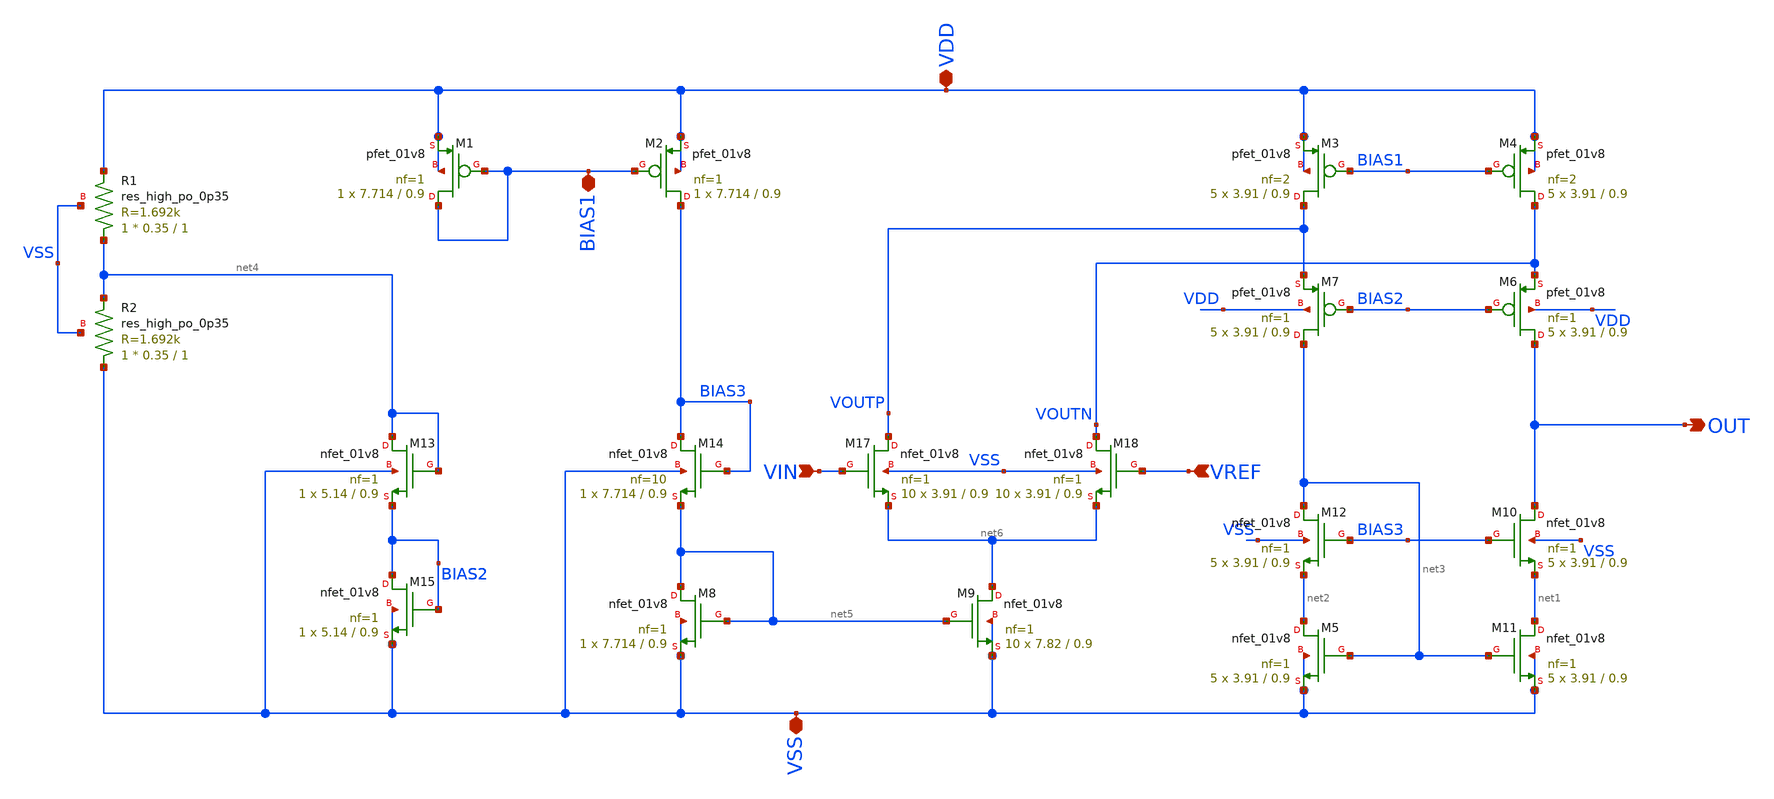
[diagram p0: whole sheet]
** sch_path: xschem/DC_DC_Converter_xschem/OTHERS/DC_DC_Converter_4/Folded_OPAMP/Folded_OPAMP_v2.sch
**.subckt Folded_OPAMP_v2 VSS VDD OUT VIN VREF BIAS1
*.iopin VSS
*.iopin VDD
*.opin OUT
*.ipin VIN
*.ipin VREF
*.iopin BIAS1
XM3 VOUTP BIAS1 VDD VDD sky130_fd_pr__pfet_01v8 L=0.9 W=3.91 nf=2 ad='int((nf+1)/2) * W/nf * 0.29' as='int((nf+2)/2) * W/nf * 0.29'
+ pd='2*int((nf+1)/2) * (W/nf + 0.29)' ps='2*int((nf+2)/2) * (W/nf + 0.29)' nrd='0.29 / W' nrs='0.29 / W'
+ sa=0 sb=0 sd=0 mult=5 m=5
XM4 VOUTN BIAS1 VDD VDD sky130_fd_pr__pfet_01v8 L=0.9 W=3.91 nf=2 ad='int((nf+1)/2) * W/nf * 0.29' as='int((nf+2)/2) * W/nf * 0.29'
+ pd='2*int((nf+1)/2) * (W/nf + 0.29)' ps='2*int((nf+2)/2) * (W/nf + 0.29)' nrd='0.29 / W' nrs='0.29 / W'
+ sa=0 sb=0 sd=0 mult=5 m=5
XM6 OUT BIAS2 VOUTN VDD sky130_fd_pr__pfet_01v8 L=0.9 W=3.91 nf=1 ad='int((nf+1)/2) * W/nf * 0.29' as='int((nf+2)/2) * W/nf * 0.29'
+ pd='2*int((nf+1)/2) * (W/nf + 0.29)' ps='2*int((nf+2)/2) * (W/nf + 0.29)' nrd='0.29 / W' nrs='0.29 / W'
+ sa=0 sb=0 sd=0 mult=5 m=5
XM7 net3 BIAS2 VOUTP VDD sky130_fd_pr__pfet_01v8 L=0.9 W=3.91 nf=1 ad='int((nf+1)/2) * W/nf * 0.29' as='int((nf+2)/2) * W/nf * 0.29'
+ pd='2*int((nf+1)/2) * (W/nf + 0.29)' ps='2*int((nf+2)/2) * (W/nf + 0.29)' nrd='0.29 / W' nrs='0.29 / W'
+ sa=0 sb=0 sd=0 mult=5 m=5
XM13 net4 net4 BIAS2 VSS sky130_fd_pr__nfet_01v8 L=0.9 W=5.14 nf=1 ad='int((nf+1)/2) * W/nf * 0.29' as='int((nf+2)/2) * W/nf * 0.29'
+ pd='2*int((nf+1)/2) * (W/nf + 0.29)' ps='2*int((nf+2)/2) * (W/nf + 0.29)' nrd='0.29 / W' nrs='0.29 / W'
+ sa=0 sb=0 sd=0 mult=1 m=1
XM14 BIAS3 BIAS3 net5 VSS sky130_fd_pr__nfet_01v8 L=0.9 W=7.714 nf=10 ad='int((nf+1)/2) * W/nf * 0.29'
+ as='int((nf+2)/2) * W/nf * 0.29' pd='2*int((nf+1)/2) * (W/nf + 0.29)' ps='2*int((nf+2)/2) * (W/nf + 0.29)'
+ nrd='0.29 / W' nrs='0.29 / W' sa=0 sb=0 sd=0 mult=1 m=1
XM15 BIAS2 BIAS2 VSS VSS sky130_fd_pr__nfet_01v8 L=0.9 W=5.14 nf=1 ad='int((nf+1)/2) * W/nf * 0.29' as='int((nf+2)/2) * W/nf * 0.29'
+ pd='2*int((nf+1)/2) * (W/nf + 0.29)' ps='2*int((nf+2)/2) * (W/nf + 0.29)' nrd='0.29 / W' nrs='0.29 / W'
+ sa=0 sb=0 sd=0 mult=1 m=1
XM17 VOUTP VIN net6 VSS sky130_fd_pr__nfet_01v8 L=0.9 W=3.91 nf=1 ad='int((nf+1)/2) * W/nf * 0.29' as='int((nf+2)/2) * W/nf * 0.29'
+ pd='2*int((nf+1)/2) * (W/nf + 0.29)' ps='2*int((nf+2)/2) * (W/nf + 0.29)' nrd='0.29 / W' nrs='0.29 / W'
+ sa=0 sb=0 sd=0 mult=10 m=10
XM18 VOUTN VREF net6 VSS sky130_fd_pr__nfet_01v8 L=0.9 W=3.91 nf=1 ad='int((nf+1)/2) * W/nf * 0.29' as='int((nf+2)/2) * W/nf * 0.29'
+ pd='2*int((nf+1)/2) * (W/nf + 0.29)' ps='2*int((nf+2)/2) * (W/nf + 0.29)' nrd='0.29 / W' nrs='0.29 / W'
+ sa=0 sb=0 sd=0 mult=10 m=10
XM10 OUT BIAS3 net1 VSS sky130_fd_pr__nfet_01v8 L=0.9 W=3.91 nf=1 ad='int((nf+1)/2) * W/nf * 0.29' as='int((nf+2)/2) * W/nf * 0.29'
+ pd='2*int((nf+1)/2) * (W/nf + 0.29)' ps='2*int((nf+2)/2) * (W/nf + 0.29)' nrd='0.29 / W' nrs='0.29 / W'
+ sa=0 sb=0 sd=0 mult=5 m=5
XM12 net3 BIAS3 net2 VSS sky130_fd_pr__nfet_01v8 L=0.9 W=3.91 nf=1 ad='int((nf+1)/2) * W/nf * 0.29' as='int((nf+2)/2) * W/nf * 0.29'
+ pd='2*int((nf+1)/2) * (W/nf + 0.29)' ps='2*int((nf+2)/2) * (W/nf + 0.29)' nrd='0.29 / W' nrs='0.29 / W'
+ sa=0 sb=0 sd=0 mult=5 m=5
XM8 net5 net5 VSS VSS sky130_fd_pr__nfet_01v8 L=0.9 W=7.714 nf=1 ad='int((nf+1)/2) * W/nf * 0.29' as='int((nf+2)/2) * W/nf * 0.29'
+ pd='2*int((nf+1)/2) * (W/nf + 0.29)' ps='2*int((nf+2)/2) * (W/nf + 0.29)' nrd='0.29 / W' nrs='0.29 / W'
+ sa=0 sb=0 sd=0 mult=1 m=1
XM9 net6 net5 VSS VSS sky130_fd_pr__nfet_01v8 L=0.9 W=7.82 nf=1 ad='int((nf+1)/2) * W/nf * 0.29' as='int((nf+2)/2) * W/nf * 0.29'
+ pd='2*int((nf+1)/2) * (W/nf + 0.29)' ps='2*int((nf+2)/2) * (W/nf + 0.29)' nrd='0.29 / W' nrs='0.29 / W'
+ sa=0 sb=0 sd=0 mult=10 m=10
XM5 net2 net3 VSS VSS sky130_fd_pr__nfet_01v8 L=0.9 W=3.91 nf=1 ad='int((nf+1)/2) * W/nf * 0.29' as='int((nf+2)/2) * W/nf * 0.29'
+ pd='2*int((nf+1)/2) * (W/nf + 0.29)' ps='2*int((nf+2)/2) * (W/nf + 0.29)' nrd='0.29 / W' nrs='0.29 / W'
+ sa=0 sb=0 sd=0 mult=5 m=5
XM11 net1 net3 VSS VSS sky130_fd_pr__nfet_01v8 L=0.9 W=3.91 nf=1 ad='int((nf+1)/2) * W/nf * 0.29' as='int((nf+2)/2) * W/nf * 0.29'
+ pd='2*int((nf+1)/2) * (W/nf + 0.29)' ps='2*int((nf+2)/2) * (W/nf + 0.29)' nrd='0.29 / W' nrs='0.29 / W'
+ sa=0 sb=0 sd=0 mult=5 m=5
XM1 BIAS1 BIAS1 VDD VDD sky130_fd_pr__pfet_01v8 L=0.9 W=7.714 nf=1 ad='int((nf+1)/2) * W/nf * 0.29' as='int((nf+2)/2) * W/nf * 0.29'
+ pd='2*int((nf+1)/2) * (W/nf + 0.29)' ps='2*int((nf+2)/2) * (W/nf + 0.29)' nrd='0.29 / W' nrs='0.29 / W'
+ sa=0 sb=0 sd=0 mult=1 m=1
XM2 BIAS3 BIAS1 VDD VDD sky130_fd_pr__pfet_01v8 L=0.9 W=7.714 nf=1 ad='int((nf+1)/2) * W/nf * 0.29' as='int((nf+2)/2) * W/nf * 0.29'
+ pd='2*int((nf+1)/2) * (W/nf + 0.29)' ps='2*int((nf+2)/2) * (W/nf + 0.29)' nrd='0.29 / W' nrs='0.29 / W'
+ sa=0 sb=0 sd=0 mult=1 m=1
XR1 net4 VDD VSS sky130_fd_pr__res_high_po_0p35 L=1 mult=1 m=1
XR2 VSS net4 VSS sky130_fd_pr__res_high_po_0p35 L=1 mult=1 m=1
**.ends
.end
